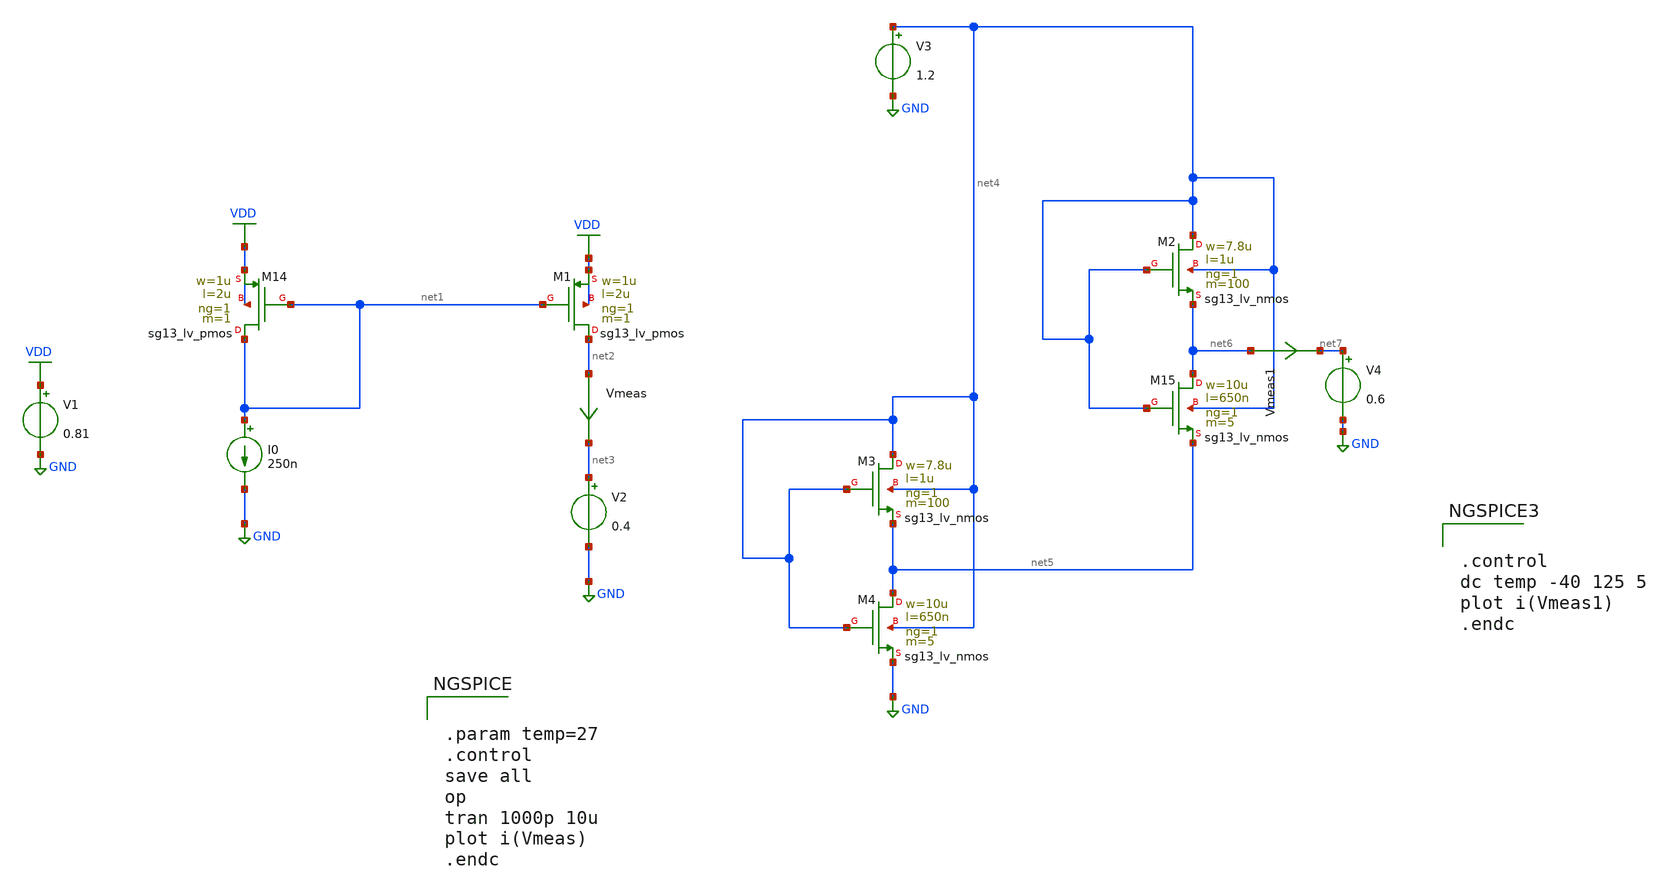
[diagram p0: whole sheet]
** sch_path: SSDOR_1.2V_v2/components/Ib_4u/CTAT_PTAT/tb_MOS.sch
**.subckt tb_MOS
V1 VDD GND 0.81
XM14 net1 net1 VDD VDD sg13_lv_pmos w=1u l=2u ng=1 m=1 mm_ok=1
I0 net1 GND 250n
XM1 net2 net1 VDD VDD sg13_lv_pmos w=1u l=2u ng=1 m=1 mm_ok=1
V2 net3 GND 0.4
Vmeas net2 net3 0
.save i(vmeas)
XM2 net4 net4 net6 net4 sg13_lv_nmos w=7.8u l=1u ng=1 m=100 mm_ok=1
XM15 net6 net4 net5 net4 sg13_lv_nmos w=10u l=650n ng=1 m=5 mm_ok=1
V3 net4 GND 1.2
V4 net7 GND 0.6
Vmeas1 net6 net7 0
.save i(vmeas1)
XM3 net4 net4 net5 net4 sg13_lv_nmos w=7.8u l=1u ng=1 m=100 mm_ok=1
XM4 net5 net4 GND net4 sg13_lv_nmos w=10u l=650n ng=1 m=5 mm_ok=1
**** begin user architecture code


** IHP models
.lib cornerMOSlv.lib mos_tt
.lib cornerMOShv.lib mos_tt
.lib cornerHBT.lib hbt_typ
.lib cornerRES.lib res_typ




.param temp=27
.control
save all
op
tran 1000p 10u
plot i(Vmeas)
.endc




.control
dc temp -40 125 5
plot i(Vmeas1)
.endc




.control
op
save all
dc temp -40 125 5
write gm.raw
.endc
.save @m.xm15.sg13_lv_nmos[gm]


**** end user architecture code
**.ends
.GLOBAL VDD
.GLOBAL GND
.end
